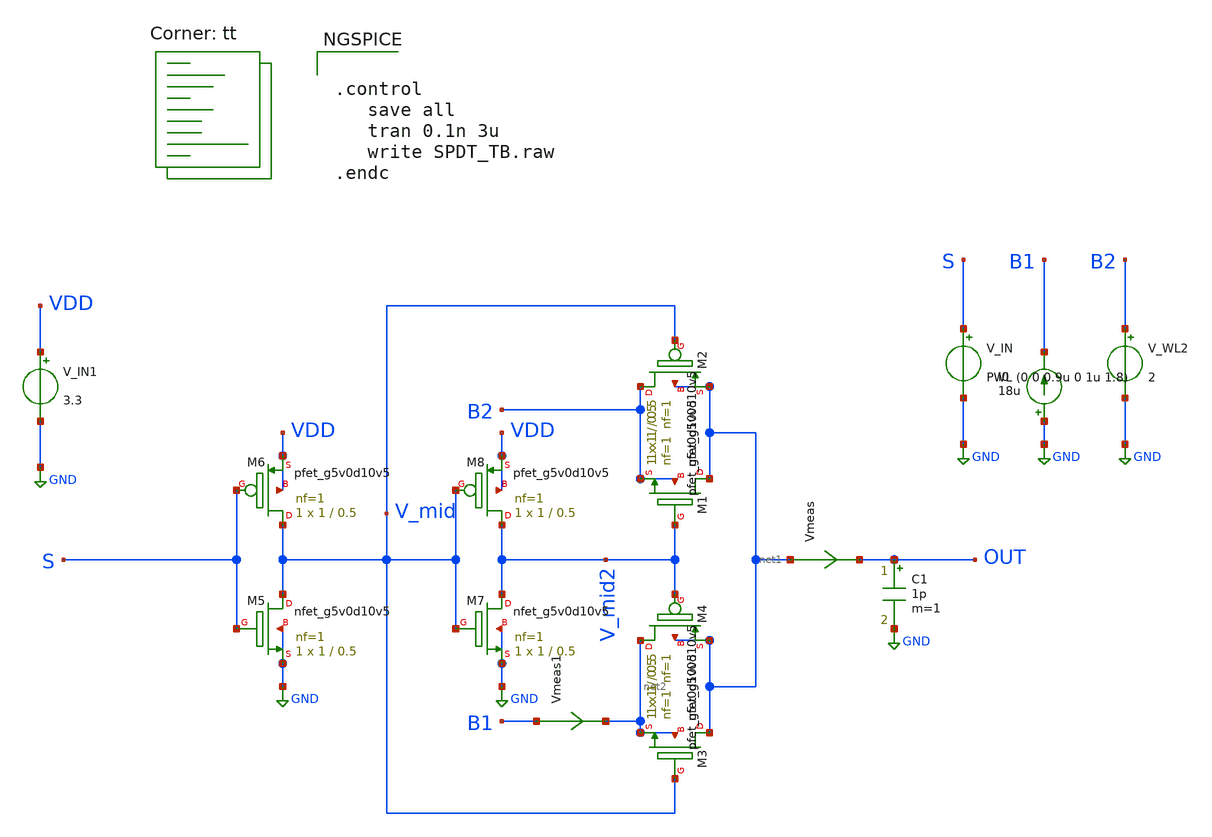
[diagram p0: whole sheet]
** sch_path: xschem/test/xschem/SPDT_TB.sch
**.subckt SPDT_TB
XM1 net1 V_mid2 B2 B2 sky130_fd_pr__nfet_g5v0d10v5 L=0.5 W=1 nf=1 ad='int((nf+1)/2) * W/nf * 0.29' as='int((nf+2)/2) * W/nf * 0.29'
+ pd='2*int((nf+1)/2) * (W/nf + 0.29)' ps='2*int((nf+2)/2) * (W/nf + 0.29)' nrd='0.29 / W' nrs='0.29 / W'
+ sa=0 sb=0 sd=0 mult=1 m=1
XM2 B2 V_mid net1 net1 sky130_fd_pr__pfet_g5v0d10v5 L=0.5 W=1 nf=1 ad='int((nf+1)/2) * W/nf * 0.29' as='int((nf+2)/2) * W/nf * 0.29'
+ pd='2*int((nf+1)/2) * (W/nf + 0.29)' ps='2*int((nf+2)/2) * (W/nf + 0.29)' nrd='0.29 / W' nrs='0.29 / W'
+ sa=0 sb=0 sd=0 mult=1 m=1
XM3 net1 V_mid net2 net2 sky130_fd_pr__nfet_g5v0d10v5 L=0.5 W=1 nf=1 ad='int((nf+1)/2) * W/nf * 0.29'
+ as='int((nf+2)/2) * W/nf * 0.29' pd='2*int((nf+1)/2) * (W/nf + 0.29)' ps='2*int((nf+2)/2) * (W/nf + 0.29)'
+ nrd='0.29 / W' nrs='0.29 / W' sa=0 sb=0 sd=0 mult=1 m=1
XM4 net2 V_mid2 net1 net1 sky130_fd_pr__pfet_g5v0d10v5 L=0.5 W=1 nf=1 ad='int((nf+1)/2) * W/nf * 0.29'
+ as='int((nf+2)/2) * W/nf * 0.29' pd='2*int((nf+1)/2) * (W/nf + 0.29)' ps='2*int((nf+2)/2) * (W/nf + 0.29)'
+ nrd='0.29 / W' nrs='0.29 / W' sa=0 sb=0 sd=0 mult=1 m=1
V_IN S GND PWL (0 0 0.9u 0 1u 1.8)
V_WL2 B2 GND 2
C1 OUT GND 1p m=1
XM5 V_mid S GND GND sky130_fd_pr__nfet_g5v0d10v5 L=0.5 W=1 nf=1 ad='int((nf+1)/2) * W/nf * 0.29' as='int((nf+2)/2) * W/nf * 0.29'
+ pd='2*int((nf+1)/2) * (W/nf + 0.29)' ps='2*int((nf+2)/2) * (W/nf + 0.29)' nrd='0.29 / W' nrs='0.29 / W'
+ sa=0 sb=0 sd=0 mult=1 m=1
XM6 V_mid S VDD VDD sky130_fd_pr__pfet_g5v0d10v5 L=0.5 W=1 nf=1 ad='int((nf+1)/2) * W/nf * 0.29' as='int((nf+2)/2) * W/nf * 0.29'
+ pd='2*int((nf+1)/2) * (W/nf + 0.29)' ps='2*int((nf+2)/2) * (W/nf + 0.29)' nrd='0.29 / W' nrs='0.29 / W'
+ sa=0 sb=0 sd=0 mult=1 m=1
V_IN1 VDD GND 3.3
XM7 V_mid2 V_mid GND GND sky130_fd_pr__nfet_g5v0d10v5 L=0.5 W=1 nf=1 ad='int((nf+1)/2) * W/nf * 0.29'
+ as='int((nf+2)/2) * W/nf * 0.29' pd='2*int((nf+1)/2) * (W/nf + 0.29)' ps='2*int((nf+2)/2) * (W/nf + 0.29)'
+ nrd='0.29 / W' nrs='0.29 / W' sa=0 sb=0 sd=0 mult=1 m=1
XM8 V_mid2 V_mid VDD VDD sky130_fd_pr__pfet_g5v0d10v5 L=0.5 W=1 nf=1 ad='int((nf+1)/2) * W/nf * 0.29'
+ as='int((nf+2)/2) * W/nf * 0.29' pd='2*int((nf+1)/2) * (W/nf + 0.29)' ps='2*int((nf+2)/2) * (W/nf + 0.29)'
+ nrd='0.29 / W' nrs='0.29 / W' sa=0 sb=0 sd=0 mult=1 m=1
Vmeas net1 OUT 0
.save i(vmeas)
Vmeas1 B1 net2 0
.save i(vmeas1)
I0 GND B1 18u
**** begin user architecture code
.lib $::SKYWATER_MODELS/sky130.lib.spice tt


.control
   save all
   tran 0.1n 3u
   write SPDT_TB.raw
.endc


**** end user architecture code
**.ends
.GLOBAL GND
.end
